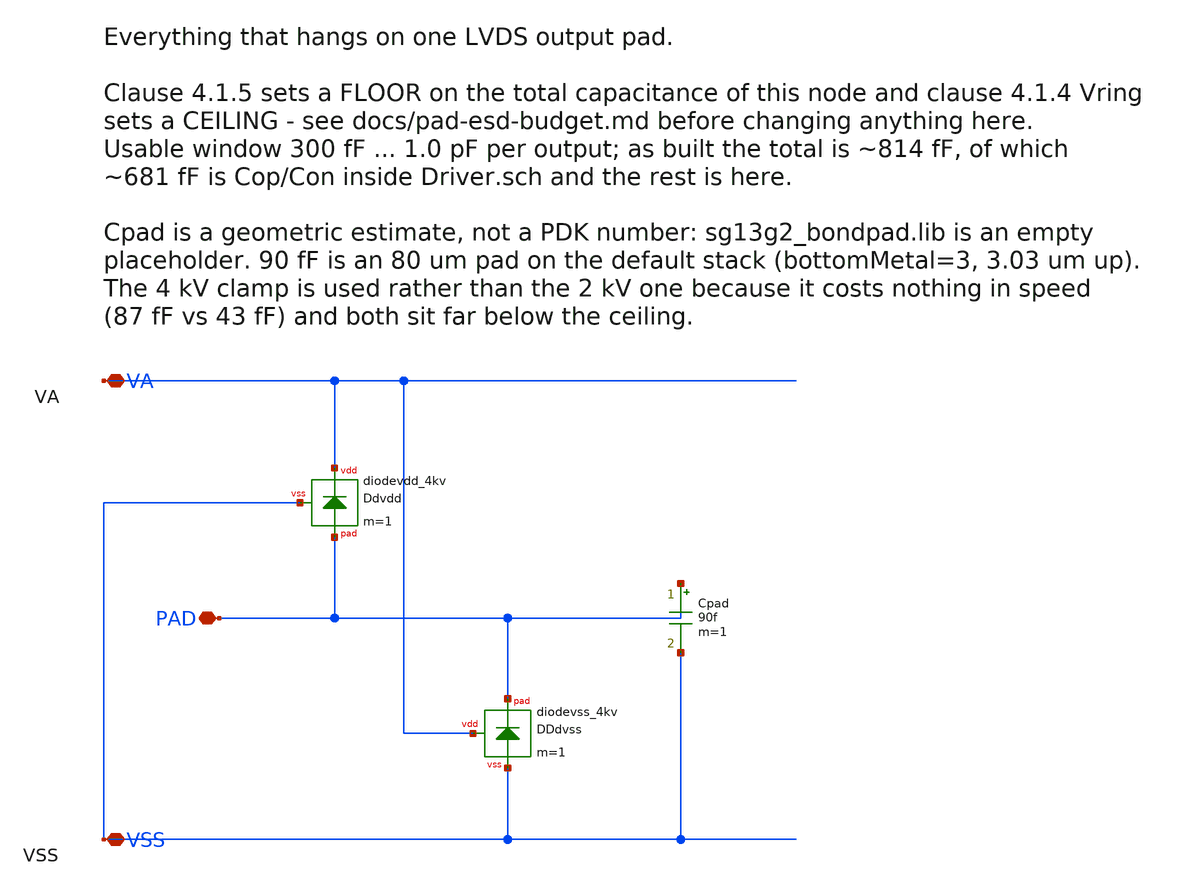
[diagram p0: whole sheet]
** sch_path: macros/lvds_tx/schematic/xschem/esdpad.sch
**.subckt esdpad PAD VA VSS
*.iopin PAD
*.iopin VA
*.iopin VSS
XDdvdd VA PAD VSS diodevdd_4kv m=1
XDdvss VA PAD VSS diodevss_4kv m=1
Cpad PAD VSS 90f m=1
**.ends
.end
